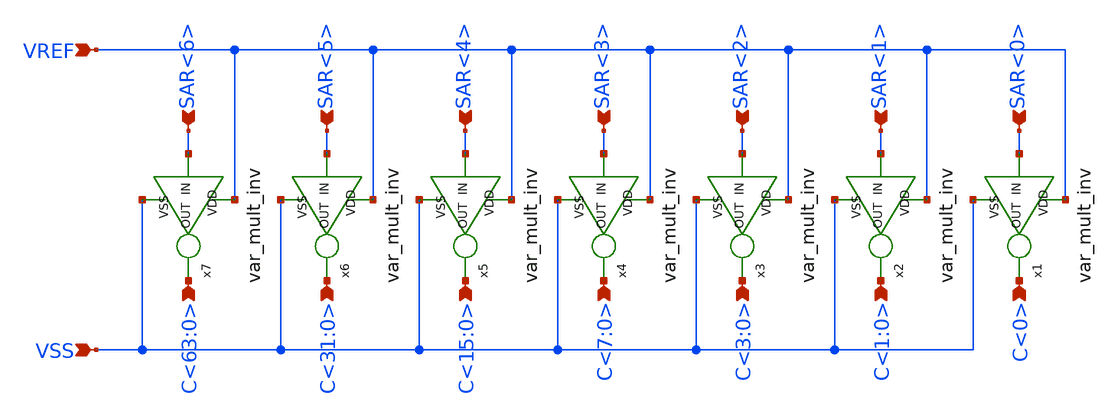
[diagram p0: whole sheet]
** sch_path: module/cdac/cdac_drv.sch
**.subckt cdac_drv VREF VSS SAR<6> SAR<5> SAR<4> SAR<3> SAR<2> SAR<1> SAR<0> C<63:0> C<31:0> C<15:0>
*+ C<7:0> C<3:0> C<1:0> C<0>
*.ipin VREF
*.ipin VSS
*.ipin SAR<6>
*.ipin SAR<5>
*.ipin SAR<4>
*.ipin SAR<3>
*.ipin SAR<2>
*.ipin SAR<1>
*.ipin SAR<0>
*.ipin C<63:0>
*.ipin C<31:0>
*.ipin C<15:0>
*.ipin C<7:0>
*.ipin C<3:0>
*.ipin C<1:0>
*.ipin C<0>
x1 VREF SAR<0> C<0> VSS var_mult_inv multp=multp multn=multn
x2 VREF SAR<1> C<1:0> VSS var_mult_inv multp=multp multn=multn
x3 VREF SAR<2> C<3:0> VSS var_mult_inv multp=multp multn=multn
x4 VREF SAR<3> C<7:0> VSS var_mult_inv multp=multp multn=multn
x5 VREF SAR<4> C<15:0> VSS var_mult_inv multp=multp multn=multn
x6 VREF SAR<5> C<31:0> VSS var_mult_inv multp=multp multn=multn
x7 VREF SAR<6> C<63:0> VSS var_mult_inv multp=multp multn=multn
**.ends
.end
